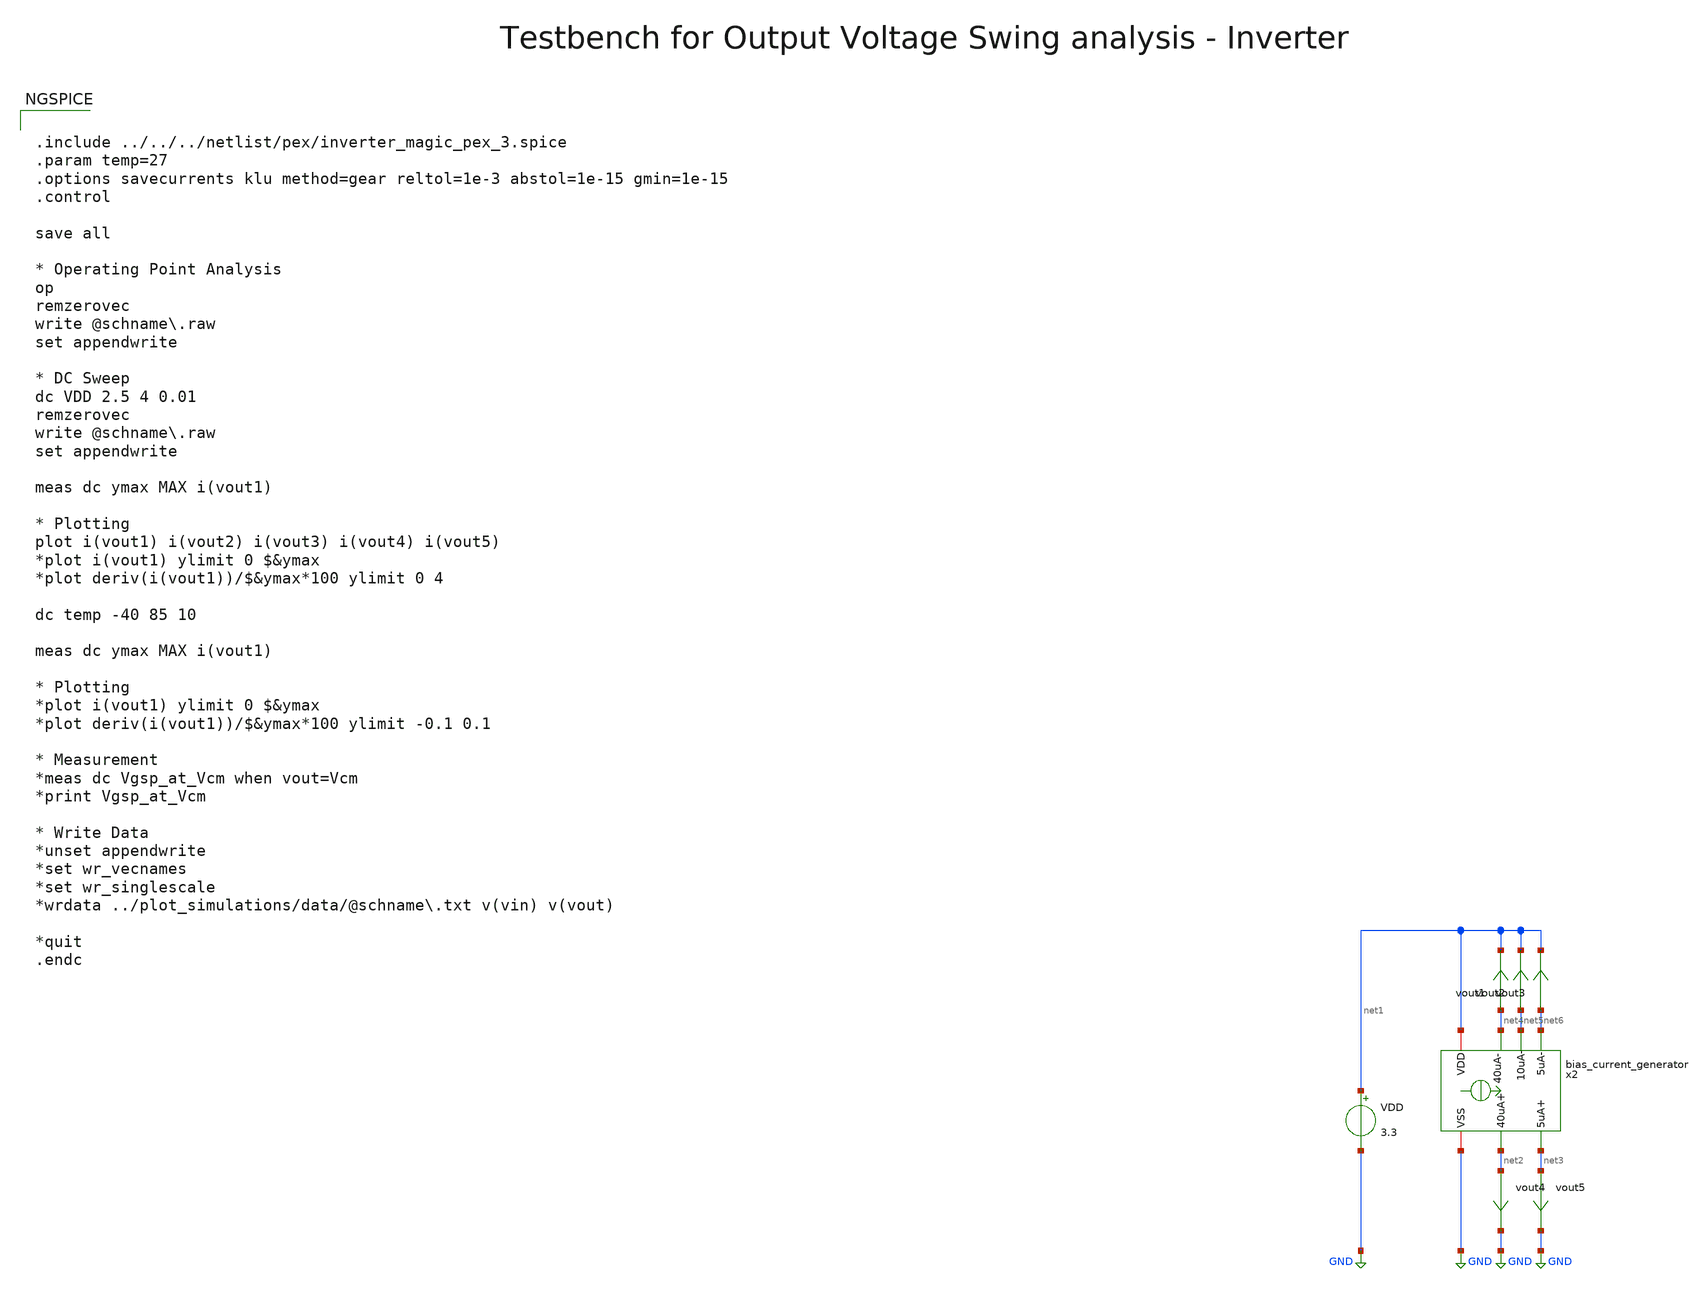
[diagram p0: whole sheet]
** sch_path: macros/heichips26_vcr/macros/switched_capacitor/testbenches/xschem/tb_bias_current_generator_dc.sch
**.subckt tb_bias_current_generator_dc
VDD net1 GND 3.3
vout1 net4 net1 0
.save i(vout1)
x2 net2 net3 net1 GND net6 net5 net4 bias_current_generator
vout2 net5 net1 0
.save i(vout2)
vout3 net6 net1 0
.save i(vout3)
vout4 net2 GND 0
.save i(vout4)
vout5 net3 GND 0
.save i(vout5)
**** begin user architecture code


.include ../../../netlist/pex/inverter_magic_pex_3.spice
.param temp=27
.options savecurrents klu method=gear reltol=1e-3 abstol=1e-15 gmin=1e-15
.control

save all

* Operating Point Analysis
op
remzerovec
write @schname\.raw
set appendwrite

* DC Sweep
dc VDD 2.5 4 0.01
remzerovec
write @schname\.raw
set appendwrite

meas dc ymax MAX i(vout1)

* Plotting
plot i(vout1) i(vout2) i(vout3) i(vout4) i(vout5)
*plot i(vout1) ylimit 0 $&ymax
*plot deriv(i(vout1))/$&ymax*100 ylimit 0 4

dc temp -40 85 10

meas dc ymax MAX i(vout1)

* Plotting
*plot i(vout1) ylimit 0 $&ymax
*plot deriv(i(vout1))/$&ymax*100 ylimit -0.1 0.1

* Measurement
*meas dc Vgsp_at_Vcm when vout=Vcm
*print Vgsp_at_Vcm

* Write Data
*unset appendwrite
*set wr_vecnames
*set wr_singlescale
*wrdata ../plot_simulations/data/@schname\.txt v(vin) v(vout)

*quit
.endc



.lib cornerMOSlv.lib mos_tt
.lib cornerMOShv.lib mos_tt
.lib cornerRES.lib res_typ
.lib cornerDIO.lib dio_tt

**** end user architecture code
**.ends

* expanding   symbol:  bias_current_generator.sym # of pins=7
** sym_path: macros/heichips26_vcr/macros/switched_capacitor/schematic/xschem/bias_current_generator.sym
** sch_path: macros/heichips26_vcr/macros/switched_capacitor/schematic/xschem/bias_current_generator.sch
.subckt bias_current_generator 40uA+ 5uA+ VDD VSS 5uA- 10uA- 40uA-
*.opin 40uA+
*.iopin VSS
*.iopin VDD
*.opin 40uA-
*.opin 10uA-
*.opin 5uA+
*.opin 5uA-
x4 VDD net1 VSS current_reference_40uA
XM11 net1 net1 VDD VDD sg13_hv_pmos w=cm_p_w l=cm_p_l ng=1 m=1 mm_ok=1
XM12 40uA+ net1 VDD VDD sg13_hv_pmos w=cm_p_w l=cm_p_l ng=1 m=1 mm_ok=1
XM13 net2 net1 VDD VDD sg13_hv_pmos w=cm_p_w l=cm_p_l ng=1 m=1 mm_ok=1
XM14 net2 net2 VSS VSS sg13_hv_nmos w=cm_n_w l=cm_n_l ng=1 m=1 mm_ok=1
XM15 40uA- net2 VSS VSS sg13_hv_nmos w=cm_n_w l=cm_n_l ng=1 m=1 mm_ok=1
XM1 net3 net1 VDD VDD sg13_hv_pmos w=cm_p_w l=cm_p_l ng=1 m=1 mm_ok=1
XM2 net3 net3 VSS VSS sg13_hv_nmos w=4*cm_n_w l=cm_n_l ng=4 m=1 mm_ok=1
XM3 10uA- net3 VSS VSS sg13_hv_nmos w=cm_n_w l=cm_n_l ng=1 m=1 mm_ok=1
XM5 net4 net3 VSS VSS sg13_hv_nmos w=cm_n_w l=cm_n_l ng=1 m=1 mm_ok=1
XM25 net4 net4 VDD VDD sg13_hv_pmos w=2*cm_p_w l=cm_p_l ng=2 m=1 mm_ok=1
XM26 net5 net4 VDD VDD sg13_hv_pmos w=cm_p_w l=cm_p_l ng=1 m=1 mm_ok=1
XM27 5uA+ net4 VDD VDD sg13_hv_pmos w=cm_p_w l=cm_p_l ng=1 m=1 mm_ok=1
XM28 net5 net5 VSS VSS sg13_hv_nmos w=cm_n_w l=cm_n_l ng=2 m=1 mm_ok=1
XM29 5uA- net5 VSS VSS sg13_hv_nmos w=cm_n_w l=cm_n_l ng=1 m=1 mm_ok=1
**** begin user architecture code


.param cm_n_w = 6u
.param cm_n_l = 5u
.param cm_p_w = 10u
.param cm_p_l = 2u


**** end user architecture code
.ends


* expanding   symbol:  current_reference_40uA.sym # of pins=3
** sym_path: macros/heichips26_vcr/macros/switched_capacitor/schematic/xschem/current_reference_40uA.sym
** sch_path: macros/heichips26_vcr/macros/switched_capacitor/schematic/xschem/current_reference_40uA.sch
.subckt current_reference_40uA VDD iout VSS
*.iopin VSS
*.iopin VDD
*.iopin iout
XM8 net2 net2 VSS VSS sg13_hv_nmos w=n_w l=n_l ng=1 m=1 mm_ok=1
XM6 net2 net1 VDD VDD sg13_hv_pmos w=p_w l=p_l ng=1 m=1 mm_ok=1
XM1 net1 net1 VDD VDD sg13_hv_pmos w=p_w l=p_l ng=1 m=1 mm_ok=1
XM3 net1 net2 net3 VSS sg13_hv_nmos w=n_w l=n_l ng=1 m=1 mm_ok=1
XR2 net4 VSS VSS rppd w=2e-6 l=21.9e-6 m=1 b=0 mm_ok=1
XM2 net1 net2 net3 VSS sg13_hv_nmos w=n_w l=n_l ng=1 m=1 mm_ok=1
XM4 net1 net2 net3 VSS sg13_hv_nmos w=n_w l=n_l ng=1 m=1 mm_ok=1
XM5 net1 net2 net3 VSS sg13_hv_nmos w=n_w l=n_l ng=1 m=1 mm_ok=1
XM7 iout net2 VSS VSS sg13_hv_nmos w=n_w l=n_l ng=1 m=1 mm_ok=1
XR3 net3 net4 VSS rsil w=0.5e-6 l=365e-6 m=1 mm_ok=1
**** begin user architecture code


.param n_w = 6u
.param n_l = 5u
.param p_w = 10u
.param p_l = 2u


**** end user architecture code
.ends

.GLOBAL GND
.end
